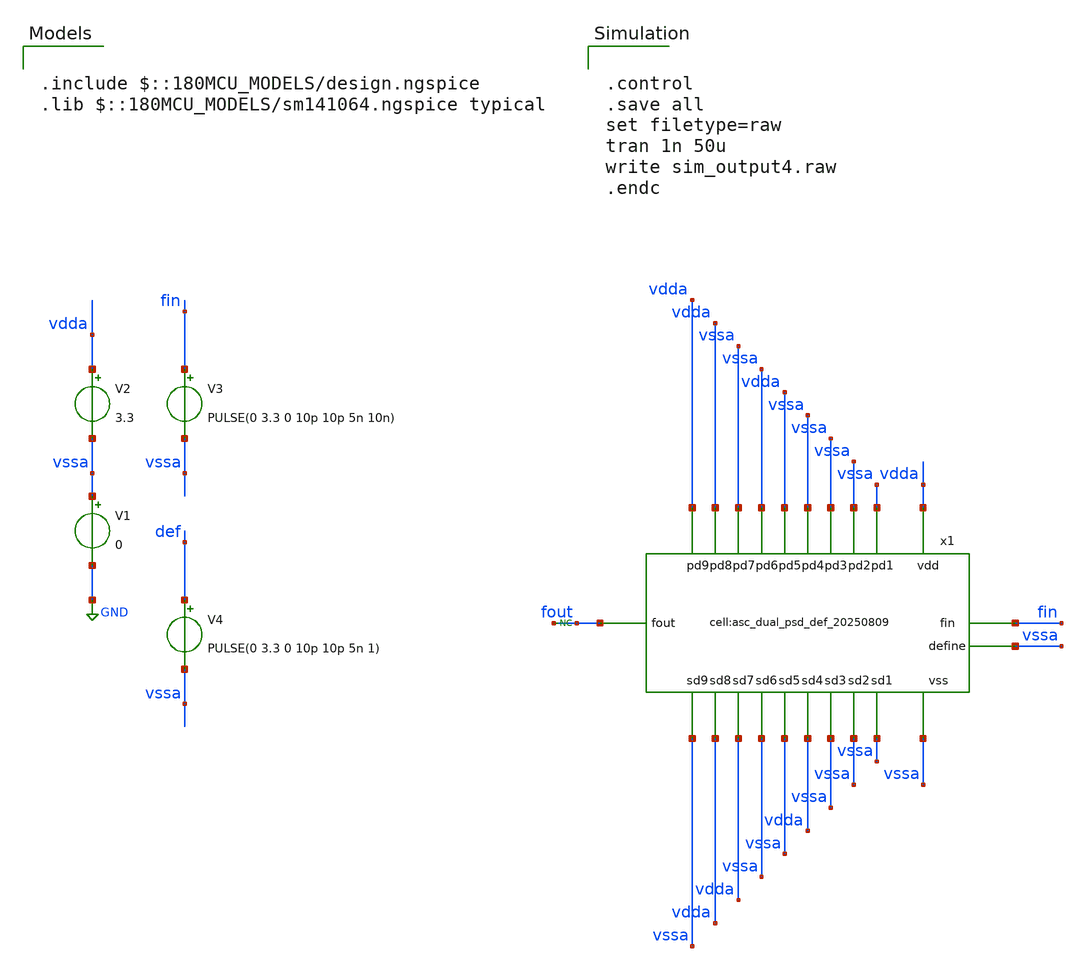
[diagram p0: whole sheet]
** sch_path: designs/libs/tb_analog/tb_asc_FM_pulse_swallow_divider_def/tb_asc_FM_pulse_swallow_divider_def.sch
**.subckt tb_asc_FM_pulse_swallow_divider_def
V1 vssa GND 0
V2 vdda vssa 3.3
V3 fin vssa PULSE(0 3.3 0 10p 10p 5n 10n)
V4 def vssa PULSE(0 3.3 0 10p 10p 5n 1)
x1 fout vssa vdda vdda vssa vssa vdda vssa vssa vssa vssa fin vdda vssa vdda vdda vssa vssa vdda
+ vssa vssa vssa vssa asc_dual_psd_def_20250809
* noconn fout
**** begin user architecture code

.include $::180MCU_MODELS/design.ngspice
.lib $::180MCU_MODELS/sm141064.ngspice typical



.control
.save all
set filetype=raw
tran 1n 50u
write sim_output4.raw
.endc


**** end user architecture code
**.ends
.GLOBAL GND
.end
